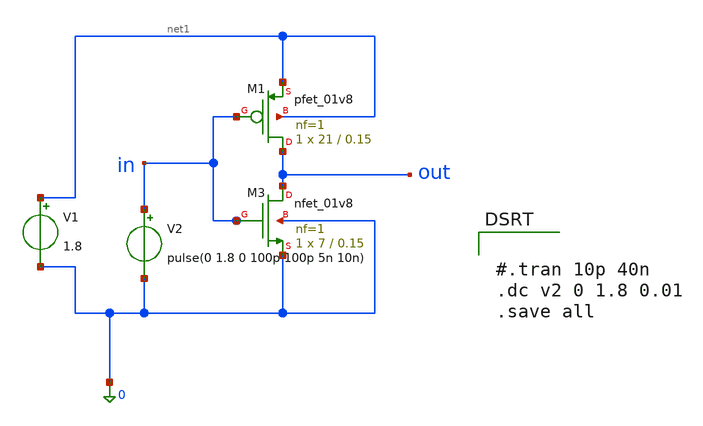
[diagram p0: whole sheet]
** sch_path: cmos_067.sch
**.subckt cmos_067
XM3 out in 0 0 sky130_fd_pr__nfet_01v8 L=0.15 W=7 nf=1 ad='int((1 + 1)/2) * 7 / 1 * 0.29' as='int((1 + 2)/2) * 7 / 1 * 0.29'
+ pd='2*int((1 + 1)/2) * (7 / 1 + 0.29)' ps='2*int((1 + 2)/2) * (7 / 1 + 0.29)' nrd='0.29 / 7 ' nrs='0.29 / 7 '
+ sa=0 sb=0 sd=0 mult=1 m=1
XM1 out in net1 net1 sky130_fd_pr__pfet_01v8 L=0.15 W=21 nf=1 ad='int((1 + 1)/2) * 21 / 1 * 0.29' as='int((1 + 2)/2) * 21 / 1 * 0.29'
+ pd='2*int((1 + 1)/2) * (21 / 1 + 0.29)' ps='2*int((1 + 2)/2) * (21 / 1 + 0.29)' nrd='0.29 / 21 ' nrs='0.29 / 21 '
+ sa=0 sb=0 sd=0 mult=1 m=1
V1 net1 0 1.8
V2 in 0 pulse(0 1.8 0 100p 100p 5n 10n)
**** begin user architecture code
 .lib /foss/pdks/sky130A/libs.tech/ngspice/sky130.lib.spice tt

.param mc_mm_switch=0
.param mc_pr_switch=1



#.tran 10p 40n
.dc v2 0 1.8 0.01
.save all


**** end user architecture code
**.ends
.end
